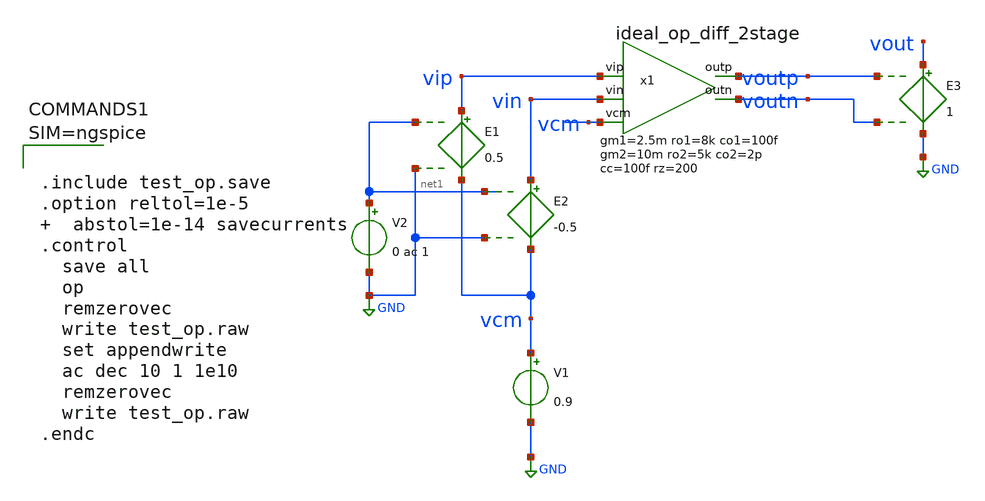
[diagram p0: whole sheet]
** sch_path: test_op.sch
**.subckt test_op
E1 vip vcm net1 GND 0.5
E2 vin vcm net1 GND -0.5
V1 vcm GND 0.9
V2 net1 GND 0 ac 1
E3 vout GND voutp voutn 1
x1 voutp vip vin voutn vcm ideal_op_diff_2stage gm1=2.5m ro1=8k co1=100f gm2=10m ro2=5k co2=2p
+ cc=100f rz=200
**** begin user architecture code



.include test_op.save
.option reltol=1e-5   abstol=1e-14 savecurrents
.control
  save all
  op
  remzerovec
  write test_op.raw
  set appendwrite
  ac dec 10 1 1e10
  remzerovec
  write test_op.raw
.endc



**** end user architecture code
**.ends

* expanding   symbol:  /home/tester/proj/modules/ideal_op_diff_2stage.sym # of pins=5
** sym_path: modules/ideal_op_diff_2stage.sym
** sch_path: modules/ideal_op_diff_2stage.sch
.subckt ideal_op_diff_2stage outp vip vin outn vcm  gm1=5m ro1=20k co1=100f gm2=10m ro2=5k co2=2p
+ cc=100f rz=200
*.ipin vip
*.ipin vin
*.opin outp
*.opin outn
*.ipin vcm
G1 net1 vcm vip vin {gm1/2}
G2 vcm net2 vip vin {gm1/2}
R1 net1 vcm {ro1} m=1
R2 vcm net2 {ro1} m=1
C1 net1 vcm {co1} m=1
C2 vcm net2 {co1} m=1
G3 outp vcm net1 vcm {gm2}
G4 vcm outn vcm net2 {gm2}
R3 outp vcm {ro2} m=1
R4 vcm outn {ro2} m=1
C3 outp vcm {co2} m=1
C4 vcm outn {co2} m=1
R5 net1 net3 {rz} m=1
C5 net3 outp {cc} m=1
R6 net2 net4 {rz} m=1
C6 net4 outn {cc} m=1
.ends

.GLOBAL GND
.end
